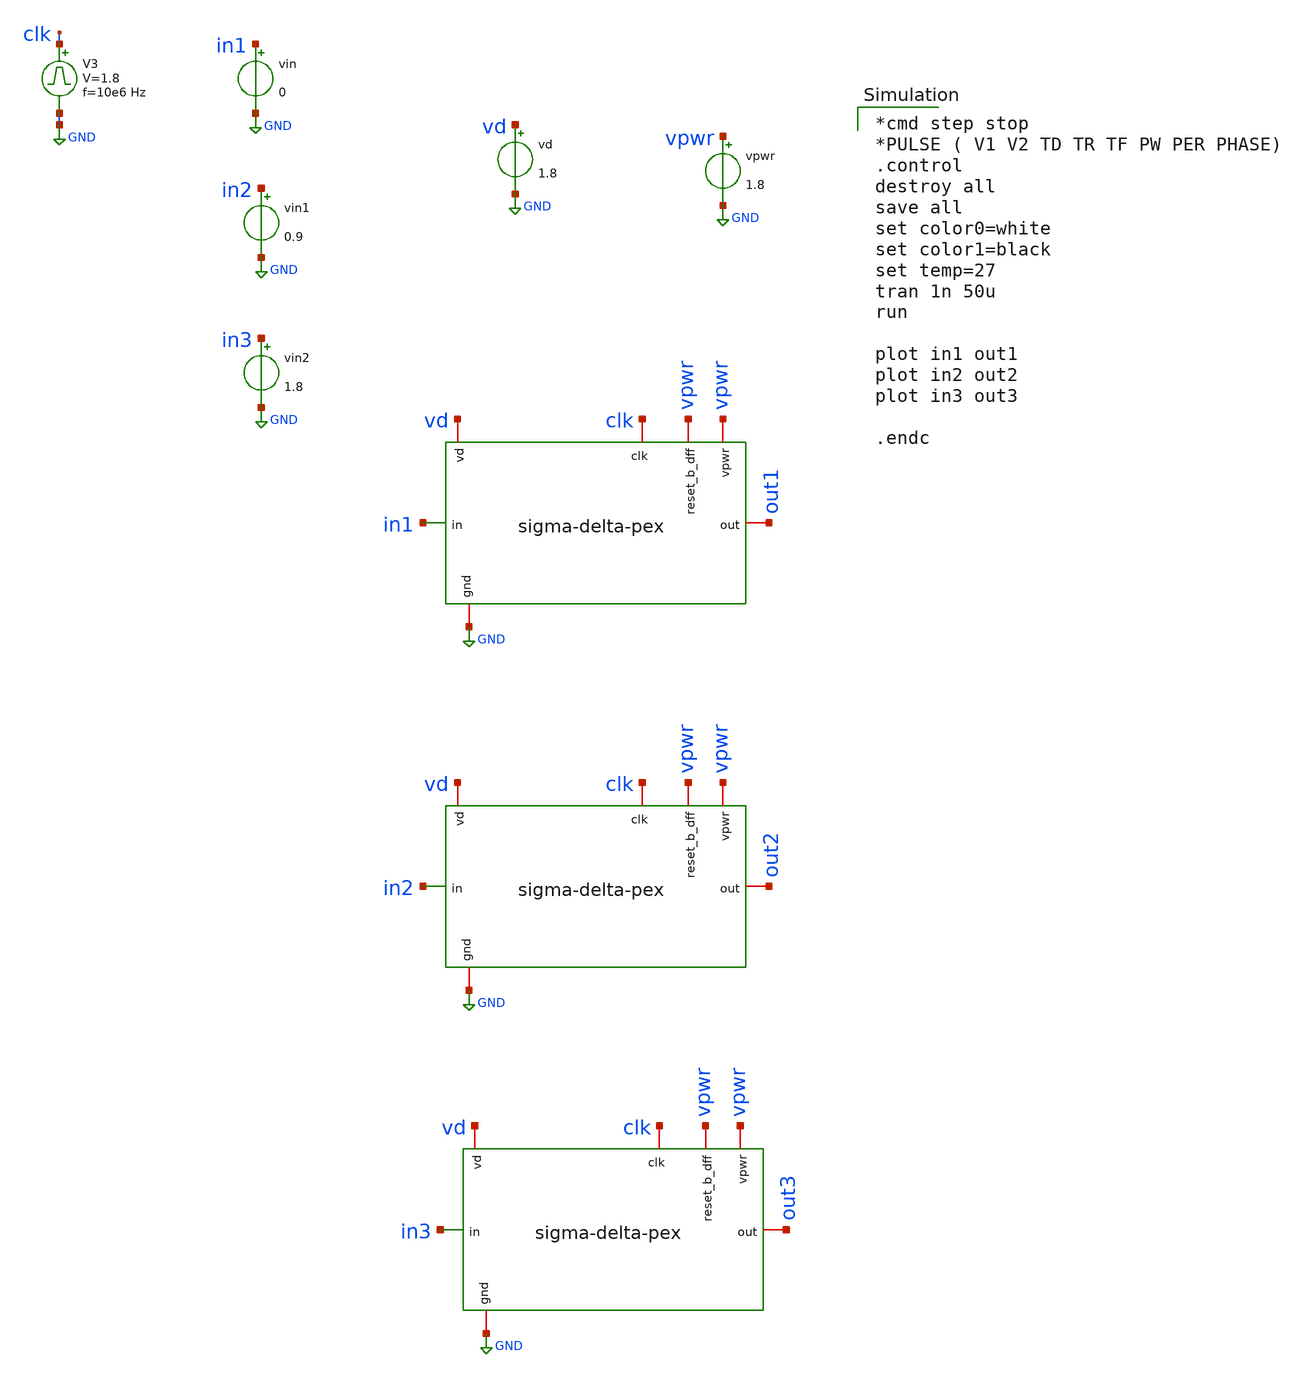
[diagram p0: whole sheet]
** sch_path: sigma-delta_modulator/xschem/sigma_tb-tran.sch
* Copyright 2020 Stefan Frederik Schippers
* Licensed under the Apache License, Version 2.0 (the "License");
* you may not use this file except in compliance with the License.
* You may obtain a copy of the License at
* https://www.apache.org/licenses/LICENSE-2.0
* Unless required by applicable law or agreed to in writing, software
* distributed under the License is distributed on an "AS IS" BASIS,
* WITHOUT WARRANTIES OR CONDITIONS OF ANY KIND, either express or implied.
* See the License for the specific language governing permissions and
* limitations under the License.
**.subckt sigma_tb-tran
vin in1 GND 0
vpwr vpwr GND 1.8
V3 clk GND pulse 0 1.8 '0.495/ 10e6 ' '0.01/10e6 ' '0.01/10e6 ' '0.49/10e6 ' '1/10e6 '
vd vd GND 1.8
x1 vpwr clk out1 in1 vpwr GND vd sigma-delta-pex
x2 vpwr clk out2 in2 vpwr GND vd sigma-delta-pex
x3 vpwr clk out3 in3 vpwr GND vd sigma-delta-pex
vin1 in2 GND 0.9
vin2 in3 GND 1.8
**** begin user architecture code

*cmd step stop
*PULSE ( V1 V2 TD TR TF PW PER PHASE)
.control
destroy all
save all
set color0=white
set color1=black
set temp=27
tran 1n 50u
run

plot in1 out1
plot in2 out2
plot in3 out3

.endc

 .lib $::SKYWATER_MODELS/sky130.lib.spice tt
.include $::SKYWATER_STDCELLS/sky130_fd_sc_hd.spice

**** end user architecture code
**.ends

* expanding   symbol:
*+  /home/hugodg/projects-sky130/temp-sensor/sigma-delta_modulator/xschem/sigma-delta-pex.sym # of pins=7
** sym_path: /home/hugodg/projects-sky130/temp-sensor/sigma-delta_modulator/xschem/sigma-delta-pex.sym
** sch_path: /home/hugodg/projects-sky130/temp-sensor/sigma-delta_modulator/xschem/sigma-delta-pex.sch
.subckt sigma-delta-pex vpwr clk out in reset_b_dff gnd vd
*.ipin in
*.iopin gnd
*.iopin clk
*.iopin out
*.iopin reset_b_dff
*.iopin vpwr
*.iopin vd
**** begin user architecture code


R0 vpwr.n4 vpwr 6628.29
R1 vpwr.n3 vpwr.n0 583.1
R2 vpwr.n4 vpwr.n2 375
R3 vpwr.n5 vpwr.n1 264.705
R4 vpwr vpwr.n3 230.841
R5 vpwr.n6 vpwr.n5 213.235
R6 vpwr.n5 vpwr.n4 185
R7 vpwr.n3 vpwr.n2 95
R8 vpwr vpwr 1.66
R9 vpwr.n7 vpwr 0.366
R10 vpwr vpwr.n7 0.033
R11 vpwr.n2 vpwr.n1 0.003
R12 vpwr.n7 vpwr.n6 0.002
R13 vpwr.n1 vpwr.n0 0.002
R14 vpwr.n6 vpwr.n0 0.002
R15 gnd.n6 gnd.n3 568.151
R16 gnd.n17 gnd.n13 568.151
R17 gnd.n20 gnd.n19 442.745
R18 gnd.n10 gnd.n9 442.728
R19 gnd.n35 gnd.n34 71.545
R20 gnd.n32 gnd.n31 71.491
R21 gnd.n40 gnd 5.358
R22 gnd gnd.n40 3.286
R23 gnd.n39 gnd 2.523
R24 gnd.n38 gnd.n37 1.736
R25 gnd.n23 gnd.n22 1.17
R26 gnd.n38 gnd.n23 0.853
R27 gnd.n23 gnd.t0 0.786
R28 gnd.n11 gnd.n1 0.65
R29 gnd.n37 gnd 0.427
R30 gnd.n20 gnd.n11 0.412
R31 gnd.n21 gnd.n20 0.399
R32 gnd.n37 gnd.n36 0.166
R33 gnd.n22 gnd.n21 0.111
R34 gnd.n34 gnd.n33 0.109
R35 gnd.n31 gnd.n30 0.109
R36 gnd.n39 gnd.n38 0.082
R37 gnd.n25 gnd.n24 0.042
R38 gnd.n27 gnd.n26 0.024
R39 gnd.n26 gnd.n25 0.02
R40 gnd.n11 gnd.n10 0.017
R41 gnd.n3 gnd.n2 0.014
R42 gnd.n13 gnd.n12 0.014
R43 gnd.n8 gnd.n7 0.006
R44 gnd.n16 gnd.n15 0.006
R45 gnd.n6 gnd.n5 0.006
R46 gnd.n18 gnd.n17 0.006
R47 gnd.n9 gnd.n8 0.006
R48 gnd.n5 gnd.n4 0.006
R49 gnd.n15 gnd.n14 0.006
R50 gnd.n19 gnd.n18 0.006
R51 gnd.n7 gnd.n6 0.002
R52 gnd.n17 gnd.n16 0.002
R53 gnd.n32 gnd.n29 0.001
R54 gnd.n29 gnd.n28 0.001
R55 gnd.n28 gnd.n27 0.001
R56 gnd.n40 gnd.n39 0.001
R57 gnd.n36 gnd.n35 0.001
R58 gnd.n36 gnd.n32 0.001
R59 gnd.n1 gnd.n0 0.001
R60 reset_b_dff.n4 reset_b_dff.t3 413.312
R61 reset_b_dff.n12 reset_b_dff.t2 344.005
R62 reset_b_dff.n1 reset_b_dff.t1 187.32
R63 reset_b_dff.n13 reset_b_dff.n12 152
R64 reset_b_dff.n4 reset_b_dff.t0 126.126
R65 reset_b_dff.n1 reset_b_dff.n0 73.206
R66 reset_b_dff.n14 reset_b_dff 14.017
R67 reset_b_dff.n5 reset_b_dff.n4 10.648
R68 reset_b_dff.n8 reset_b_dff.n7 9.3
R69 reset_b_dff.n11 reset_b_dff.n10 9.3
R70 reset_b_dff.n12 reset_b_dff.n11 9.3
R71 reset_b_dff.n12 reset_b_dff.n1 9.159
R72 reset_b_dff.n15 reset_b_dff 7.772
R73 reset_b_dff.n9 reset_b_dff.n2 4.65
R74 reset_b_dff.n14 reset_b_dff 4.533
R75 reset_b_dff reset_b_dff.n13 3.113
R76 reset_b_dff.n15 reset_b_dff.n14 3.033
R77 reset_b_dff reset_b_dff.n6 2.366
R78 reset_b_dff.n13 reset_b_dff.n0 1.556
R79 reset_b_dff.n7 reset_b_dff.n2 1.556
R80 reset_b_dff.n11 reset_b_dff.n0 1.383
R81 reset_b_dff.n11 reset_b_dff.n2 1.383
R82 reset_b_dff.n7 reset_b_dff 1.383
R83 reset_b_dff.n6 reset_b_dff 0.58
R84 reset_b_dff.n5 reset_b_dff 0.271
R85 reset_b_dff.n3 reset_b_dff 0.195
R86 reset_b_dff.n6 reset_b_dff.n5 0.082
R87 reset_b_dff.n16 reset_b_dff.n15 0.045
R88 reset_b_dff.n10 reset_b_dff.n3 0.026
R89 reset_b_dff.n8 reset_b_dff 0.025
R90 reset_b_dff.n9 reset_b_dff.n8 0.011
R91 reset_b_dff.n10 reset_b_dff.n9 0.01
R92 reset_b_dff.n16 reset_b_dff 0.008
R93 reset_b_dff.n3 reset_b_dff 0.006
R94 reset_b_dff reset_b_dff.n16 0.005
R95 clk.n0 clk.t0 294.554
R96 clk.n0 clk.t1 211.008
R97 clk.n1 clk.n0 76
R98 clk.n1 clk 10.422
R99 clk.n1 clk 8.987
R100 clk clk.n1 2.011
R101 out out 4.827
C0 x1/a_1283_21# Q 0.02fF
C1 m1_n2930_5790# m1_n1710_5800# 0.02fF
C2 out_comp clk 0.07fF
C3 reset_b_dff out 0.04fF
C4 gnd x1/a_1847_47# 0.02fF
C5 in_comp reset_b_dff 0.02fF
C6 gnd in 0.15fF
C7 gnd m1_n1550_4170# 0.01fF
C8 gnd clk 0.06fF
C9 vd x1/a_1847_47# 0.01fF
C10 out x1/a_761_289# 0.02fF
C11 out Q 0.12fF
C12 out_comp x1/a_543_47# 0.01fF
C13 vd clk 0.03fF
C14 in_comp Q 0.27fF
C15 x1/a_27_47# vpwr 0.03fF
C16 gnd out_comp 0.34fF
C17 x1/a_1108_47# out_comp 0.01fF
C18 gnd m1_n1890_4160# -0.03fF
C19 x1/a_193_47# out 0.04fF
C20 in vpwr 0.02fF
C21 gnd m1_n2050_5780# 0.01fF
C22 vd out_comp 0.70fF
C23 gnd x1/a_1108_47# 0.01fF
C24 clk vpwr 0.07fF
C25 m1_n2050_5780# m1_n3250_5800# 0.02fF
C26 x1/a_27_47# Q 0.01fF
C27 m1_n3420_4160# gnd 0.04fF
C28 vd gnd 0.66fF
C29 gnd m1_n3250_5800# 0.01fF
C30 gnd m1_n1400_5790# 0.03fF
C31 x1/a_1283_21# out 0.03fF
C32 out_comp vpwr 0.10fF
C33 m1_n1550_4170# Q 0.04fF
C34 reset_b_dff out_comp 0.22fF
C35 gnd vpwr 0.16fF
C36 m1_n2930_5790# in_comp 0.01fF
C37 gnd reset_b_dff 0.13fF
C38 reset_b_dff x1/a_1108_47# 0.01fF
C39 gnd m1_n1710_5800# 0.01fF
C40 vd vpwr 0.05fF
C41 x1/a_761_289# out_comp 0.01fF
C42 Q out_comp 0.02fF
C43 m1_n1890_4160# Q 0.03fF
C44 vd reset_b_dff 0.24fF
C45 m1_n1400_5790# m1_n1710_5800# 0.02fF
C46 gnd Q 0.27fF
C47 x1/a_1108_47# Q 0.01fF
C48 x1/a_193_47# out_comp 0.03fF
C49 x1/a_27_47# out 0.08fF
C50 vd Q 0.01fF
C51 reset_b_dff vpwr 0.01fF
C52 x1/a_1847_47# out 0.02fF
C53 in in_comp 0.14fF
C54 x1/a_1283_21# out_comp 0.02fF
C55 out clk 0.14fF
C56 in_comp m1_n1550_4170# 0.12fF
C57 x1/a_448_47# out_comp -0.02fF
C58 Q vpwr 0.18fF
C59 gnd x1/a_1283_21# 0.02fF
C60 reset_b_dff Q 0.02fF
C61 vd x1/a_1283_21# 0.02fF
C62 out out_comp 0.31fF
C63 out x1/a_543_47# 0.02fF
C64 in_comp out_comp 0.43fF
C65 m1_n2930_5790# m1_n2050_5780# 0.06fF
C66 m1_n1890_4160# in_comp 0.18fF
C67 gnd m1_n2930_5790# 0.01fF
C68 in_comp m1_n3070_4170# 0.19fF
C69 x1/a_27_47# clk 0.03fF
C70 in_comp m1_n2050_5780# 0.01fF
C71 gnd out 0.07fF
C72 out x1/a_1108_47# 0.02fF
C73 gnd in_comp 0.78fF
C74 vd out 0.07fF
C75 m1_n3420_4160# in_comp 0.14fF
C76 vd in_comp 0.22fF
C77 x1/a_193_47# Q 0.01fF
C78 x1/a_27_47# out_comp 0.09fF
C79 gnd x1/a_27_47# -0.02fF
C80 out vpwr 0.38fF
C81 in_comp 0 7.34fF
C82 gnd.t0 0 59.96fF
C83 gnd.n0 0 1.56fF $ **FLOATING
C84 gnd.n1 0 0.14fF $ **FLOATING
C85 gnd.n2 0 0.11fF $ **FLOATING
C86 gnd.n3 0 1.53fF $ **FLOATING
C87 gnd.n4 0 0.09fF $ **FLOATING
C88 gnd.n5 0 0.11fF $ **FLOATING
C89 gnd.n6 0 1.30fF $ **FLOATING
C90 gnd.n7 0 1.30fF $ **FLOATING
C91 gnd.n8 0 0.11fF $ **FLOATING
C92 gnd.n9 0 0.09fF $ **FLOATING
C93 gnd.n10 0 0.05fF $ **FLOATING
C94 gnd.n11 0 0.16fF $ **FLOATING
C95 gnd.n12 0 0.11fF $ **FLOATING
C96 gnd.n13 0 1.53fF $ **FLOATING
C97 gnd.n14 0 0.09fF $ **FLOATING
C98 gnd.n15 0 0.11fF $ **FLOATING
C99 gnd.n16 0 1.30fF $ **FLOATING
C100 gnd.n17 0 1.30fF $ **FLOATING
C101 gnd.n18 0 0.11fF $ **FLOATING
C102 gnd.n19 0 0.09fF $ **FLOATING
C103 gnd.n20 0 0.20fF $ **FLOATING
C104 gnd.n21 0 1.66fF $ **FLOATING
C105 gnd.n22 0 0.32fF $ **FLOATING
C106 gnd.n23 0 1.73fF $ **FLOATING
C107 gnd.n24 0 0.03fF $ **FLOATING
C108 gnd.n25 0 0.03fF $ **FLOATING
C109 gnd.n27 0 0.19fF $ **FLOATING
C110 gnd.n28 0 0.03fF $ **FLOATING
C111 gnd.n29 0 0.01fF $ **FLOATING
C112 gnd.n30 0 0.17fF $ **FLOATING
C113 gnd.n31 0 0.02fF $ **FLOATING
C114 gnd.n32 0 0.02fF $ **FLOATING
C115 gnd.n33 0 0.17fF $ **FLOATING
C116 gnd.n34 0 0.02fF $ **FLOATING
C117 gnd.n35 0 0.02fF $ **FLOATING
C118 gnd.n36 0 0.11fF $ **FLOATING
C119 gnd.n37 0 0.56fF $ **FLOATING
C120 gnd.n38 0 0.49fF $ **FLOATING
C121 gnd.n39 0 0.29fF $ **FLOATING
C122 gnd.n40 0 0.24fF $ **FLOATING
C123 vpwr.n0 0 0.04fF $ **FLOATING
C124 vpwr.n2 0 0.03fF $ **FLOATING
C125 vpwr.n3 0 2.03fF $ **FLOATING
C126 vpwr.n4 0 0.06fF $ **FLOATING
C127 vpwr.n6 0 0.03fF $ **FLOATING
C128 vpwr.n7 0 0.93fF $ **FLOATING
C129 m1_n2930_5790# 0 0.75fF
C130 m1_n3070_4170# 0 0.70fF
C131 m1_n3250_5800# 0 0.64fF
C132 m1_n3420_4160# 0 0.65fF
C133 in 0 1.30fF
C134 m1_n3590_5800# 0 0.86fF
C135 m1_n1400_5790# 0 0.81fF
C136 m1_n1550_4170# 0 0.70fF
C137 m1_n1710_5800# 0 0.65fF
C138 m1_n1890_4160# 0 0.74fF
C139 m1_n2050_5780# 0 0.80fF
C140 out_comp 0 2.24fF
C141 vd 0 7.26fF
C142 out 0 0.41fF
C143 Q 0 1.90fF
C144 gnd 0 15.27fF
C145 reset_b_dff 0 1.53fF
C146 clk 0 0.75fF
C147 vpwr 0 4.81fF
C148 x1/a_448_47# 0 0.01fF
C149 x1/a_1847_47# 0 0.14fF
C150 x1/a_1108_47# 0 0.13fF
C151 x1/a_1283_21# 0 0.46fF
C152 x1/a_543_47# 0 0.14fF
C153 x1/a_761_289# 0 0.11fF
C154 x1/a_193_47# 0 0.24fF
C155 x1/a_27_47# 0 0.41fF


**** end user architecture code
XC1 in_comp gnd sky130_fd_pr__cap_mim_m3_1 W=27.196 L=27.196 MF=1 m=1
XR2 Q in_comp gnd sky130_fd_pr__res_xhigh_po_0p35 L=36 mult=1 m=1
XR1 in_comp in gnd sky130_fd_pr__res_xhigh_po_0p35 L=36 mult=1 m=1
XN1 out_comp in_comp gnd gnd sky130_fd_pr__nfet_01v8 L=0.15 W=1 nf=1 ad='int((nf+1)/2) * W/nf * 0.29'
+ as='int((nf+2)/2) * W/nf * 0.29' pd='2*int((nf+1)/2) * (W/nf + 0.29)' ps='2*int((nf+2)/2) * (W/nf + 0.29)'
+ nrd='0.29 / W' nrs='0.29 / W' sa=0 sb=0 sd=0 mult=1 m=1
XP1 out_comp in_comp vd vd sky130_fd_pr__pfet_01v8 L=0.15 W=3 nf=1 ad='int((nf+1)/2) * W/nf * 0.29' as='int((nf+2)/2) * W/nf * 0.29'
+ pd='2*int((nf+1)/2) * (W/nf + 0.29)' ps='2*int((nf+2)/2) * (W/nf + 0.29)' nrd='0.29 / W' nrs='0.29 / W'
+ sa=0 sb=0 sd=0 mult=1 m=1
x1 clk out_comp reset_b_dff GND GND VPWR VPWR Q out sky130_fd_sc_hd__dfrbp_1
**** begin user architecture code

.include /usr/local/share/pdk/sky130A/libs.ref/sky130_fd_sc_hd/spice/sky130_fd_sc_hd.spice


**** end user architecture code
.ends

.GLOBAL GND
.end
